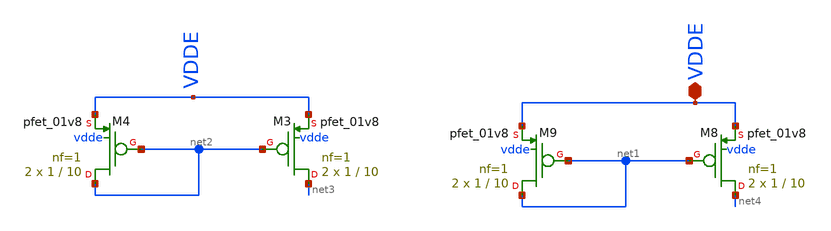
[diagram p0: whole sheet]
** sch_path: magic/pmos_current_bgr_2.sch
**.subckt pmos_current_bgr_2 VDDE
*.iopin VDDE
XM8 net4 net1 VDDE vdde sky130_fd_pr__pfet_01v8 L=10 W=1 nf=1 ad='int((nf+1)/2) * W/nf * 0.29' as='int((nf+2)/2) * W/nf * 0.29'
+ pd='2*int((nf+1)/2) * (W/nf + 0.29)' ps='2*int((nf+2)/2) * (W/nf + 0.29)' nrd='0.29 / W' nrs='0.29 / W'
+ sa=0 sb=0 sd=0 mult=2 m=2
XM9 net1 net1 VDDE vdde sky130_fd_pr__pfet_01v8 L=10 W=1 nf=1 ad='int((nf+1)/2) * W/nf * 0.29' as='int((nf+2)/2) * W/nf * 0.29'
+ pd='2*int((nf+1)/2) * (W/nf + 0.29)' ps='2*int((nf+2)/2) * (W/nf + 0.29)' nrd='0.29 / W' nrs='0.29 / W'
+ sa=0 sb=0 sd=0 mult=2 m=2
XM3 net3 net2 VDDE vdde sky130_fd_pr__pfet_01v8 L=10 W=1 nf=1 ad='int((nf+1)/2) * W/nf * 0.29' as='int((nf+2)/2) * W/nf * 0.29'
+ pd='2*int((nf+1)/2) * (W/nf + 0.29)' ps='2*int((nf+2)/2) * (W/nf + 0.29)' nrd='0.29 / W' nrs='0.29 / W'
+ sa=0 sb=0 sd=0 mult=2 m=2
XM4 net2 net2 VDDE vdde sky130_fd_pr__pfet_01v8 L=10 W=1 nf=1 ad='int((nf+1)/2) * W/nf * 0.29' as='int((nf+2)/2) * W/nf * 0.29'
+ pd='2*int((nf+1)/2) * (W/nf + 0.29)' ps='2*int((nf+2)/2) * (W/nf + 0.29)' nrd='0.29 / W' nrs='0.29 / W'
+ sa=0 sb=0 sd=0 mult=2 m=2
**.ends
.end
